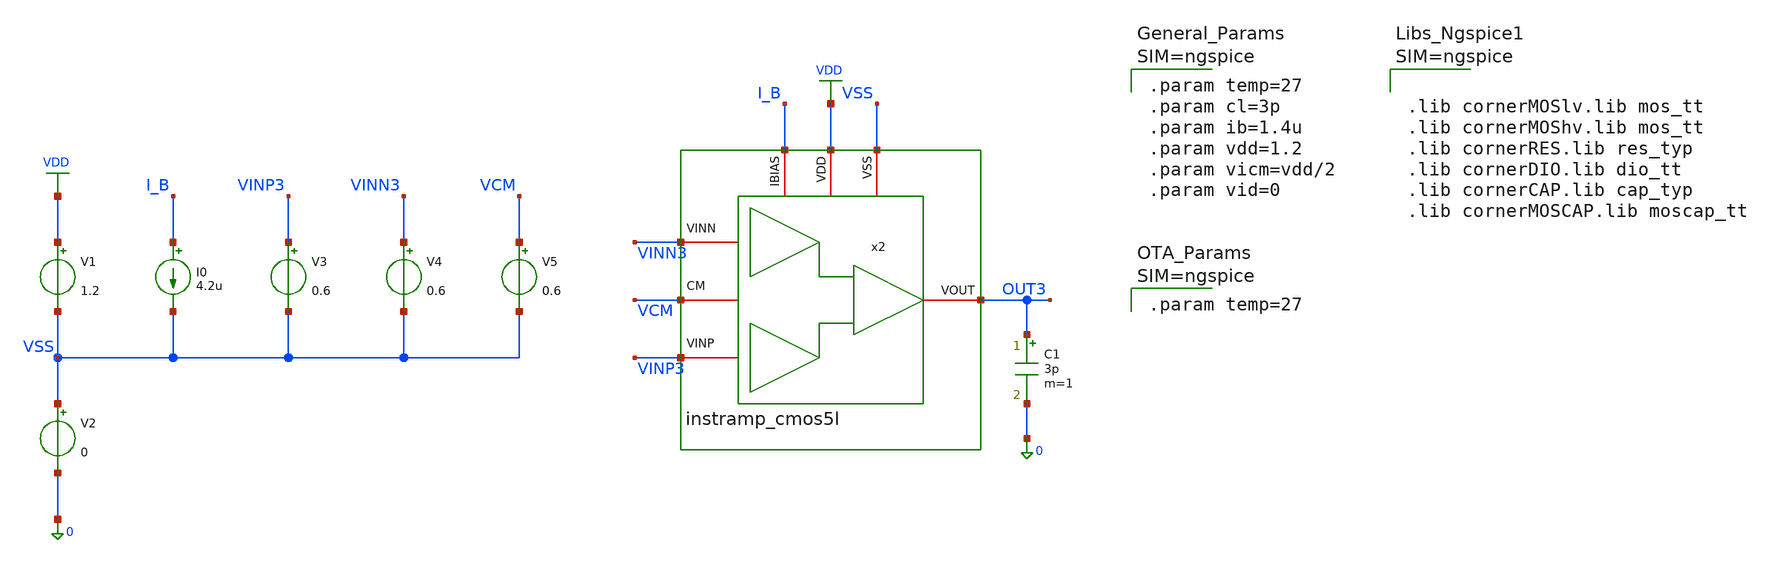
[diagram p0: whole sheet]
** sch_path: xschem/instramp_cmos5l/tb/tb_instramp_cmos5l_TRAN_small/tb_instramp_cmos5l_TRAN_small.sch
**.subckt tb_instramp_cmos5l_TRAN_small
C1 OUT3 0 3p m=1
I0 I_B VSS 4.2u
V1 VDD VSS 1.2
V2 VSS 0 0
V3 VINP3 VSS 0.6
x2 VSS VDD I_B VINN3 OUT3 VINP3 VCM instramp_cmos5l
V4 VINN3 VSS 0.6
V5 VCM VSS 0.6
**** begin user architecture code



.lib cornerMOSlv.lib mos_tt
.lib cornerMOShv.lib mos_tt
.lib cornerRES.lib res_typ
.lib cornerDIO.lib dio_tt
.lib cornerCAP.lib cap_typ
.lib cornerMOSCAP.lib moscap_tt





.param temp=27
.param cl=3p
.param ib=1.4u
.param vdd=1.2
.param vicm=vdd/2
.param vid=0





.param temp=27





.control
save all
shell mkdir -p result

* SMALL-SIGNAL TRANSIENT
* Stimulus: 1 uV (peak) 10 Hz sine on 0.6 V common
alter @v3 sin = [ 0.6 1u 10 ]

tran 1m 1

let v_ins  = v(vinp3)
let v_outs = v(out3)

* Gain and mean output level over the last 5 periods
meas tran vo_pp pp v(out3) from=0.5 to=1
meas tran vi_pp pp v(vinp3) from=0.5 to=1
meas tran vo_avg avg v(out3) from=0.5 to=1

* Save output waveforms to the specified rawfile
write ./result/tb_instramp_cmos5l_tran_small.raw v_ins v_outs

echo "======================================================="
echo "  Small-signal gain (pp/pp) : " $&vo_pp " / " $&vi_pp
echo "  Mean output level         : " $&vo_avg " V"
echo "======================================================="

plot v_outs
.endc


**** end user architecture code
**.ends

* expanding   symbol:
*+  /foss/designs/sg13cmos5l_spma_ip__instramp/xschem/instramp_cmos5l/instramp_cmos5l.sym # of pins=7
** sym_path: /foss/designs/sg13cmos5l_spma_ip__instramp/xschem/instramp_cmos5l/instramp_cmos5l.sym
** sch_path: /foss/designs/sg13cmos5l_spma_ip__instramp/xschem/instramp_cmos5l/instramp_cmos5l.sch
.subckt instramp_cmos5l VSS VDD IBIAS VINN VOUT VINP CM
*.iopin VDD
*.iopin IBIAS
*.iopin VSS
*.iopin CM
*.iopin VOUT
*.iopin VINN
*.iopin VINP
x1 VSS IBIAS VDD net3 VINP net4 ota_cmos5l
x2 VSS IBIAS VDD net1 VINN net2 ota_cmos5l
x3 VSS IBIAS VDD net5 net6 VOUT ota_cmos5l
XR1 net4 net6 VSS rhigh w=0.5e-6 l=2e-6 m=1 b=0 mm_ok=1
XR2 net2 net5 VSS rhigh w=0.5e-6 l=2e-6 m=1 b=0 mm_ok=1
XR3 net6 CM VSS rhigh w=0.5e-6 l=8*2.23e-6 m=1 b=0 mm_ok=1
XR4 net5 VOUT VSS rhigh w=0.5e-6 l=8*2.23e-6 m=1 b=0 mm_ok=1
XR7 net2 net1 VSS rhigh w=0.5e-6 l=2e-6 m=1 b=0 mm_ok=1
XR8 net4 net3 VSS rhigh w=0.5e-6 l=2e-6 m=1 b=0 mm_ok=1
.ends


* expanding   symbol:  /foss/designs/sg13cmos5l_spma_ip__instramp/xschem/ota_cmos5l/ota_cmos5l.sym #
*+ of pins=6
** sym_path: xschem/output_buffer/ota_cmos5l.sym
** sch_path: xschem/output_buffer/ota_cmos5l.sch
.subckt ota_cmos5l VSS IBIAS VDD VINN VINP VOUT
*.iopin IBIAS
*.iopin VDD
*.iopin VSS
*.iopin VOUT
*.iopin VINP
*.iopin VINN
XM6 IBIAS IBIAS VDD VDD sg13_lv_pmos w={wbias} l={lbias} ng=1 m={m6} mm_ok=1
XM7 net1 IBIAS VDD VDD sg13_lv_pmos w={wbias} l={lbias} ng=1 m={m7} mm_ok=1
XM8 VOUT IBIAS VDD VDD sg13_lv_pmos w={wbias} l={lbias} ng=1 m={m8} mm_ok=1
XM1 net2 VINN net1 VDD sg13_lv_pmos w={winpair} l={linpair} ng=1 m=1 mm_ok=1
XM2 net3 VINP net1 VDD sg13_lv_pmos w={winpair} l={linpair} ng=1 m=1 mm_ok=1
XM3 net2 net2 VSS VSS sg13_lv_nmos w={wload} l={lload} ng=1 m=1 mm_ok=1
XM4 net3 net2 VSS VSS sg13_lv_nmos w={wload} l={lload} ng=1 m=1 mm_ok=1
XM5 VOUT net3 VSS VSS sg13_lv_nmos w={wcs} l={lcs} ng=1 m=1 mm_ok=1
XR1 net3 net4 VSS rhigh w=0.5e-6 l=1.95e-6 m=1 b=0 mm_ok=1
.save v(vinp)
.save v(vinn)
.save v(vout)
XC2 VOUT net4 cap_cmomi w=15e-6 l=15e-6 mmin=1 mmax=4 feed=double subblock=0 m=5 mm_ok=1
**** begin user architecture code


.param temp=27
.param lbias=0.15u wbias=0.15u
.param m6=1 m7=4 m8=8
.param linpair=3u winpair=20u
.param lload=5u wload=10u
.param lcs=3u wcs=20u
.param Cc=2p



**** end user architecture code
XC1 VOUT net4 cap_cmomi w=15e-6 l=15e-6 mmin=1 mmax=4 feed=double subblock=0 m=4 mm_ok=1
.ends

.GLOBAL VDD
.end
